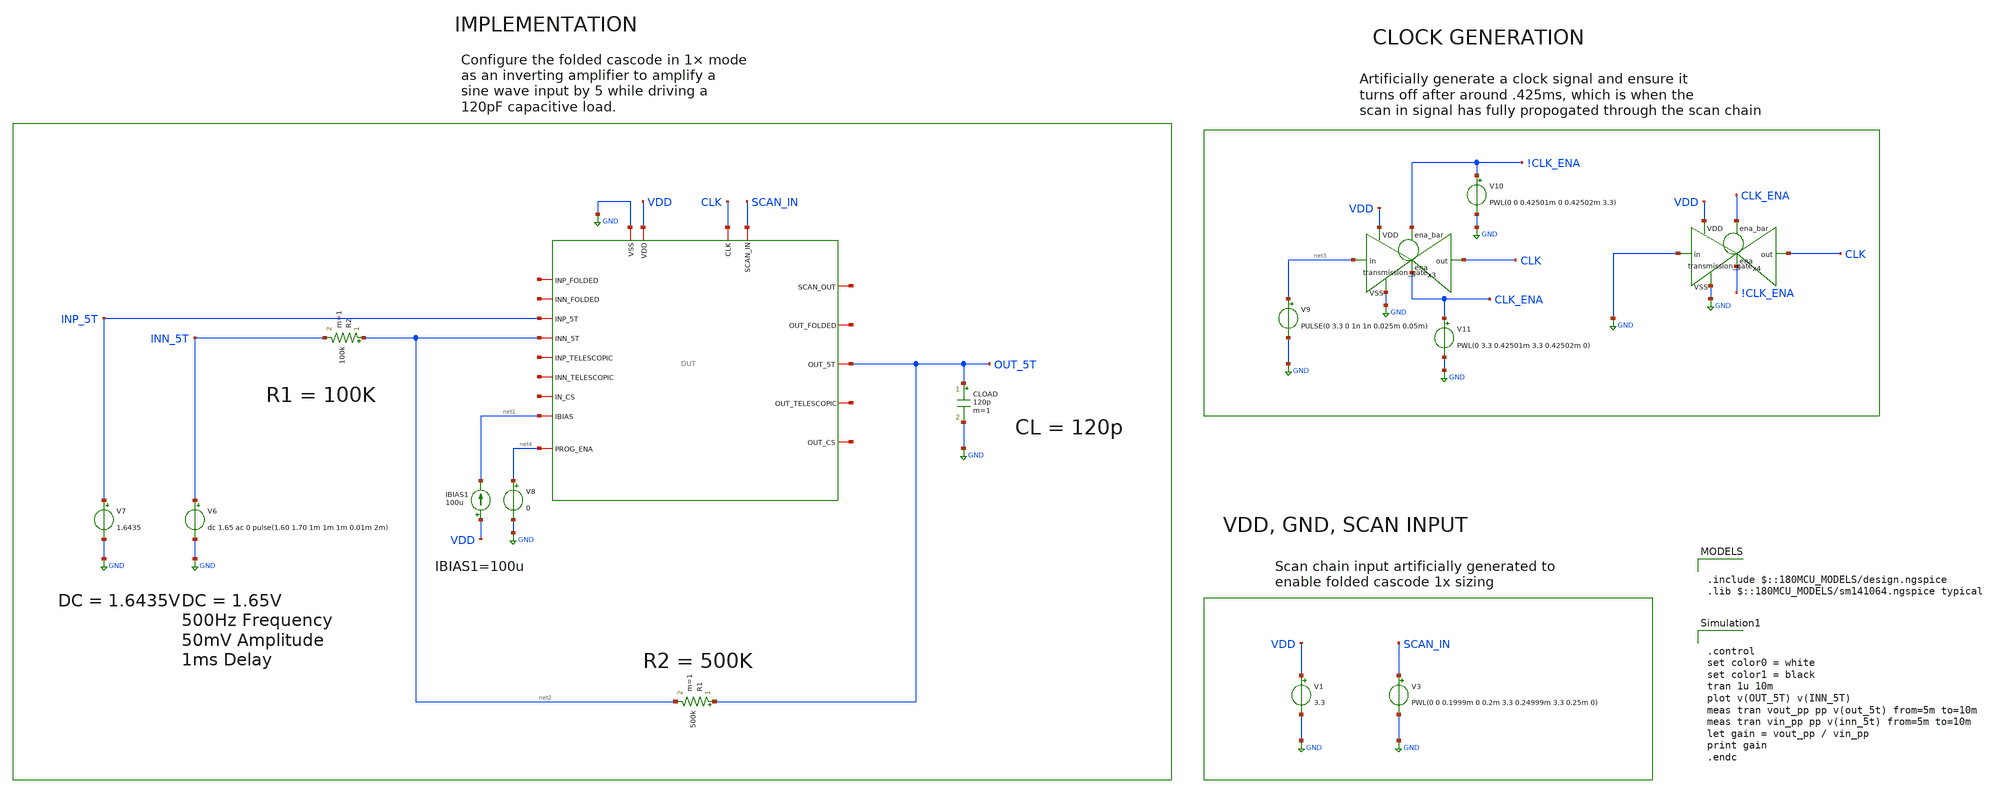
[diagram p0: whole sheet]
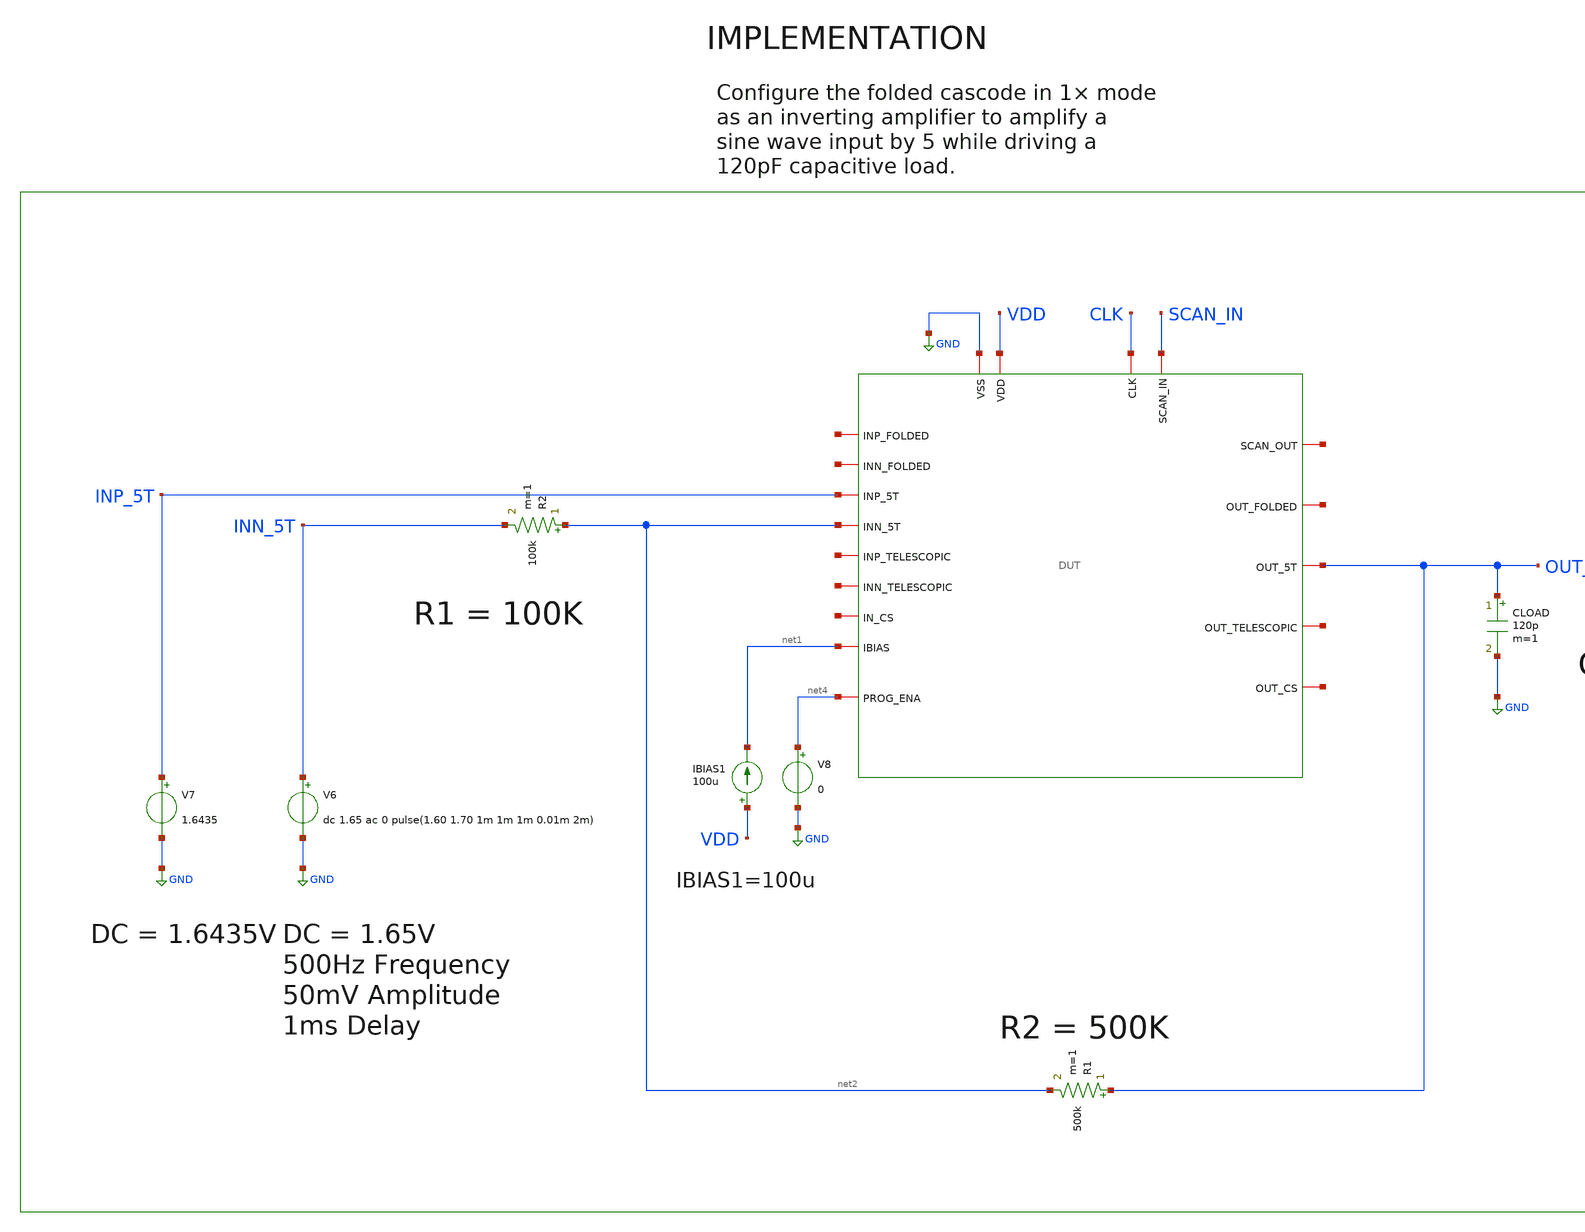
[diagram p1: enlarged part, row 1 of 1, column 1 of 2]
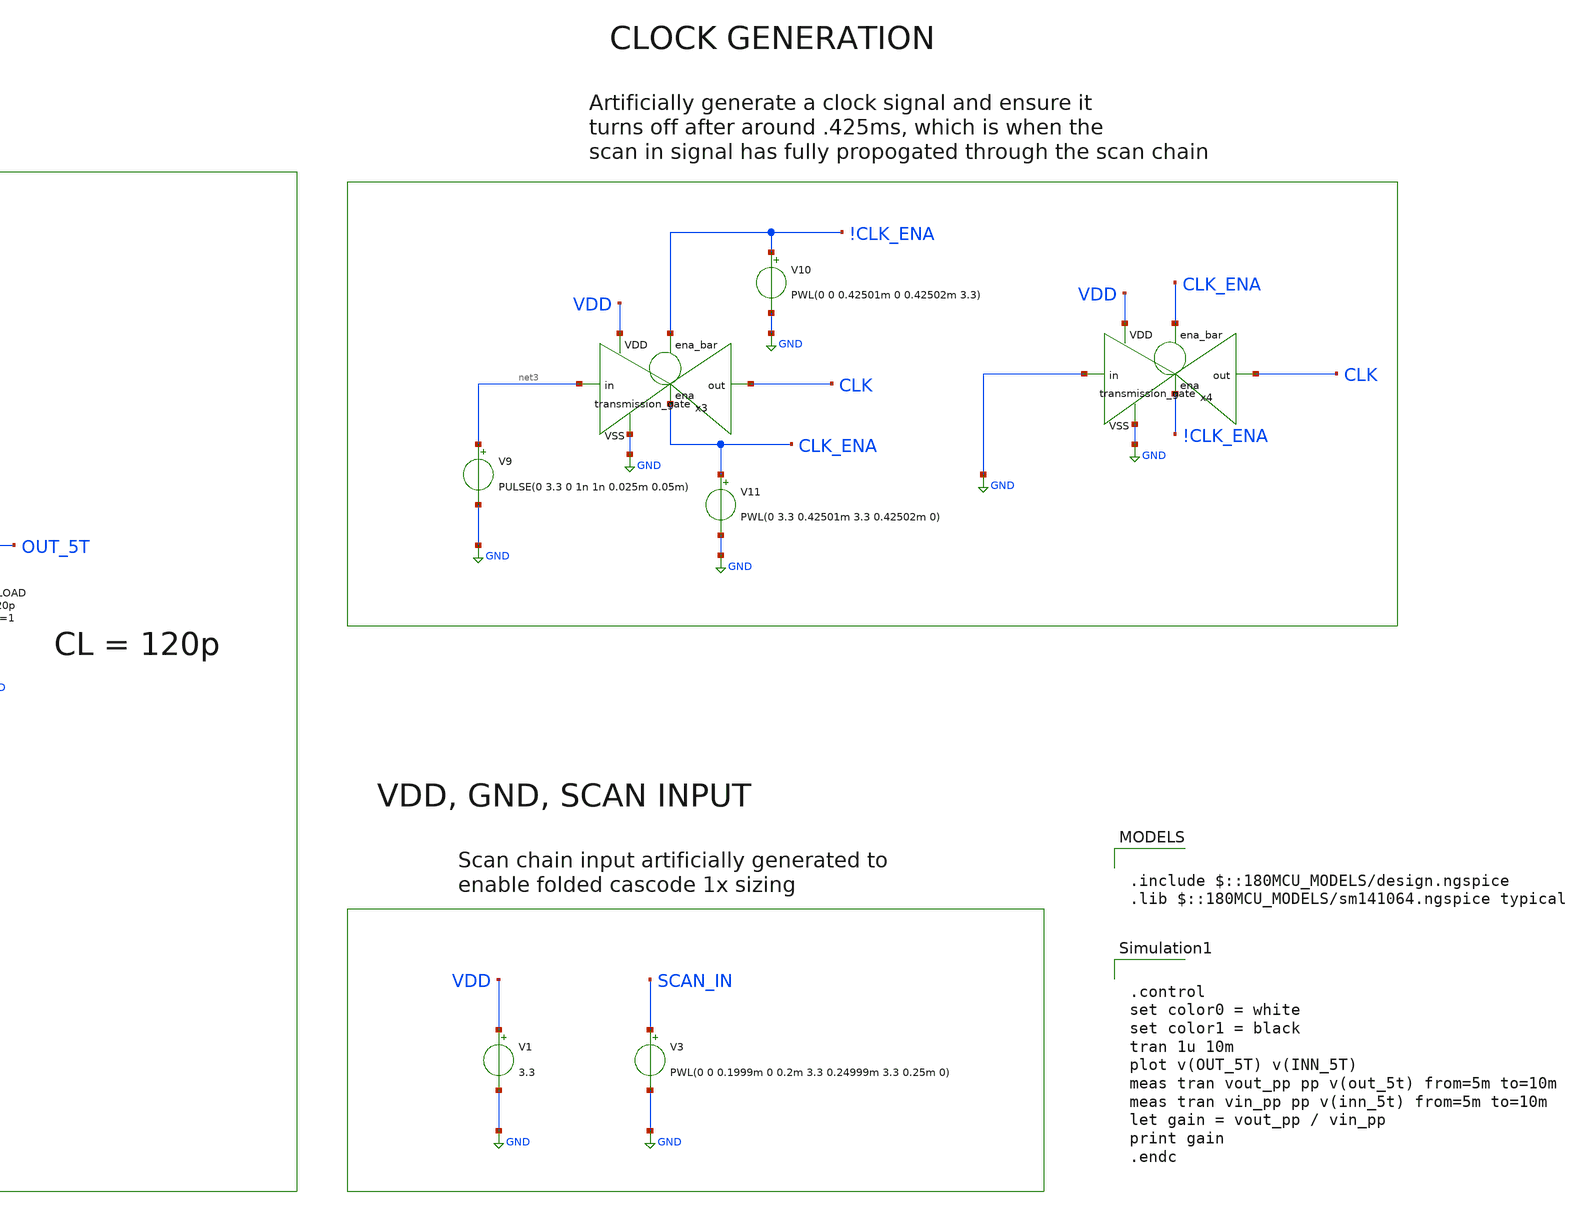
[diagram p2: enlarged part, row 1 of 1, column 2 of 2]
** sch_path: designs/libs/core_tb/sl/ota_5t/5t_inverting_triangle_1x.sch
**.subckt 5t_inverting_triangle_1x
V3 SCAN_IN GND PWL(0 0 0.1999m 0 0.2m 3.3 0.24999m 3.3 0.25m 0)
V1 VDD GND 3.3
IBIAS1 VDD net1 100u
V7 INP_5T GND 1.6435
CLOAD OUT_5T GND 120p m=1
R2 net2 INN_5T 100k m=1
V6 INN_5T GND dc 1.65 ac 0 pulse(1.60 1.70 1m 1m 1m 0.01m 2m)
R1 OUT_5T net2 500k m=1
x1 CLK net5 SCAN_IN GND VDD net6 net7 OUT_5T net1 net8 INP_5T net2 net9 net10 net11 net12 net13 net4
+ DUT
V9 net3 GND PULSE(0 3.3 0 1n 1n 0.025m 0.05m)
x3 !CLK_ENA VDD CLK net3 GND CLK_ENA transmission_gate
V10 !CLK_ENA GND PWL(0 0 0.42501m 0 0.42502m 3.3)
V11 CLK_ENA GND PWL(0 3.3 0.42501m 3.3 0.42502m 0)
x4 CLK_ENA VDD CLK GND GND !CLK_ENA transmission_gate
V8 net4 GND 0
**** begin user architecture code

.include $::180MCU_MODELS/design.ngspice
.lib $::180MCU_MODELS/sm141064.ngspice typical



.control
set color0 = white
set color1 = black
tran 1u 10m
plot v(OUT_5T) v(INN_5T)
meas tran vout_pp pp v(out_5t) from=5m to=10m
meas tran vin_pp pp v(inn_5t) from=5m to=10m
let gain = vout_pp / vin_pp
print gain
.endc


**** end user architecture code
**.ends
.GLOBAL GND
.end
